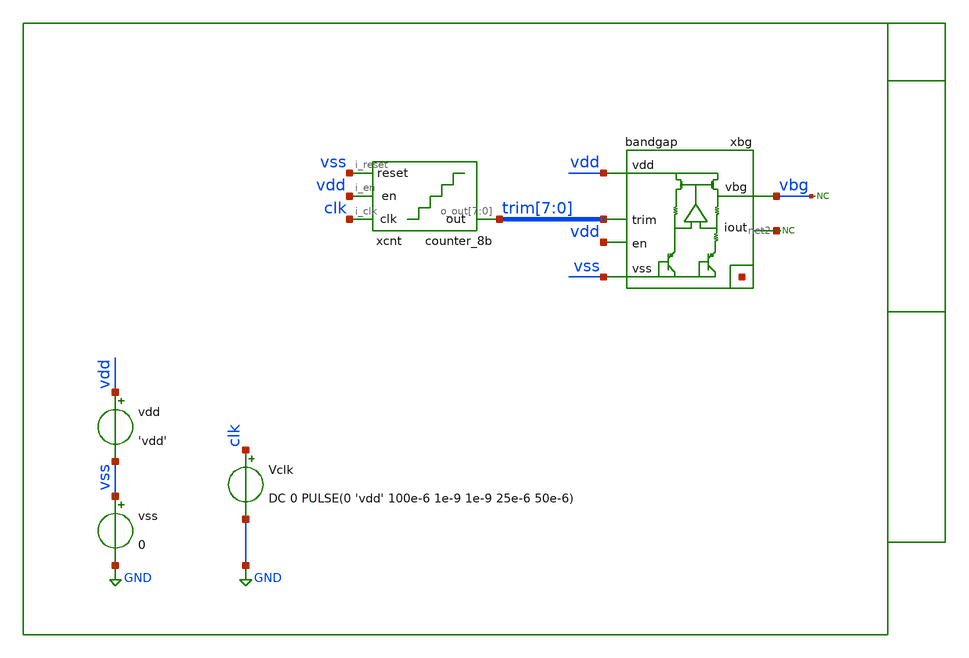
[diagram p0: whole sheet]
** sch_path: xschem/tb/bandgap_cm/bandgap/tr_bandgap_trim.sch
**.subckt tr_bandgap_trim
vss vss GND 0
vdd vdd vss 'vdd'
Vclk clk GND DC 0 PULSE(0 'vdd' 100e-6 1e-9 1e-9 25e-6 50e-6)
xbg vdd vbg vss net1[7] net1[6] net1[5] net1[4] net1[3] net1[2] net1[1] net1[0] trim[7] trim[6]
+ trim[5] trim[4] trim[3] trim[2] trim[1] trim[0] net2 vdd bandgap
* noconn vbg
xcnt vss vdd clk trim[7] trim[6] trim[5] trim[4] trim[3] trim[2] trim[1] trim[0] counter_8b
* noconn #net2
**** begin user architecture code

* Control

.param vdd = 3.3
.param cl=500e-15

.temp = 27
.options reltol = 1e-3

.control

save all
tran 1u 12.85m
gnuplot p1 vbg

.endc
.end


 * Includes
.include $::DESIGN_PATH/xschem/digital/cmos_cells_digital.sp
.include $::DESIGN_PATH/xschem/digital/counter_8b/counter_8b.sp

 * Model Corners

.include $::CORNERS/ngspice/tt.spice
*.include $::CORNERS/ngspice/ff.spice
*.include $::CORNERS/ngspice/ss.spice
*.include $::CORNERS/ngspice/sf.spice
*.include $::CORNERS/ngspice/fs.spice

**** end user architecture code
**.ends
.GLOBAL GND
.end
